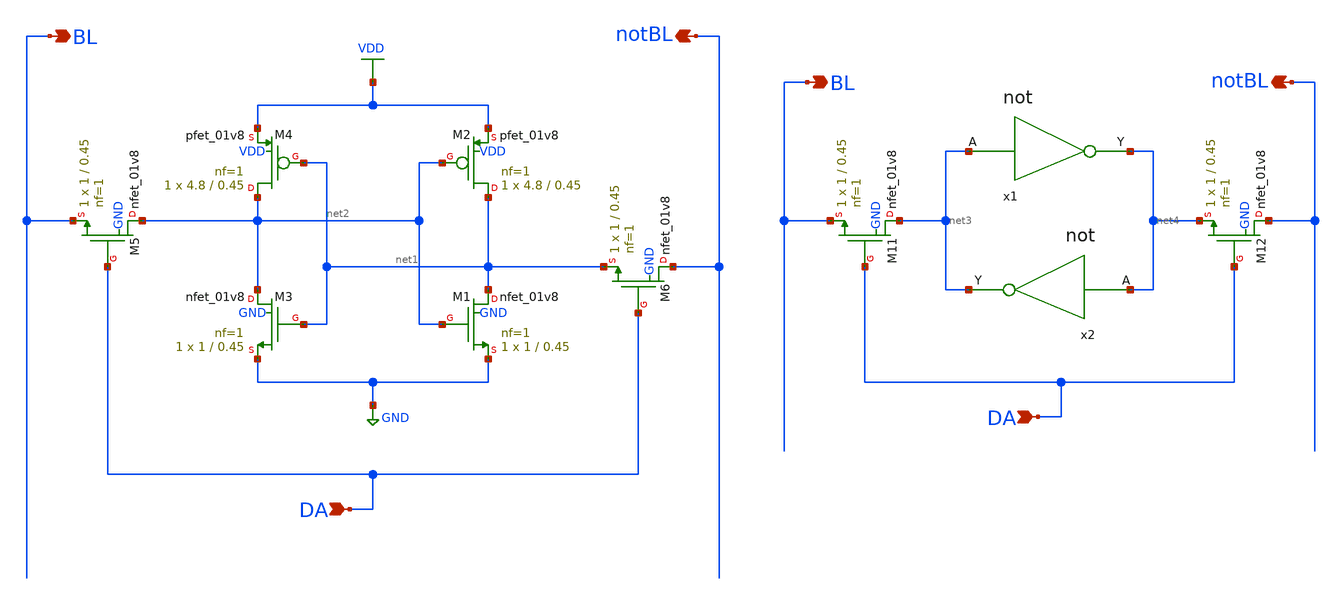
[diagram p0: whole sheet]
** sch_path: Circuiti/memories/s_RAM.sch
**.subckt s_RAM DA BL notBL DA BL notBL
*.ipin DA
*.opin BL
*.opin notBL
*.ipin DA
*.opin BL
*.opin notBL
XM1 net1 net2 GND GND sky130_fd_pr__nfet_01v8 L=0.45 W=1 nf=1 ad='int((nf+1)/2) * W/nf * 0.29' as='int((nf+2)/2) * W/nf * 0.29'
+ pd='2*int((nf+1)/2) * (W/nf + 0.29)' ps='2*int((nf+2)/2) * (W/nf + 0.29)' nrd='0.29 / W' nrs='0.29 / W'
+ sa=0 sb=0 sd=0 mult=1 m=1
XM2 net1 net2 VDD VDD sky130_fd_pr__pfet_01v8 L=0.45 W=4.8 nf=1 ad='int((nf+1)/2) * W/nf * 0.29' as='int((nf+2)/2) * W/nf * 0.29'
+ pd='2*int((nf+1)/2) * (W/nf + 0.29)' ps='2*int((nf+2)/2) * (W/nf + 0.29)' nrd='0.29 / W' nrs='0.29 / W'
+ sa=0 sb=0 sd=0 mult=1 m=1
XM3 net2 net1 GND GND sky130_fd_pr__nfet_01v8 L=0.45 W=1 nf=1 ad='int((nf+1)/2) * W/nf * 0.29' as='int((nf+2)/2) * W/nf * 0.29'
+ pd='2*int((nf+1)/2) * (W/nf + 0.29)' ps='2*int((nf+2)/2) * (W/nf + 0.29)' nrd='0.29 / W' nrs='0.29 / W'
+ sa=0 sb=0 sd=0 mult=1 m=1
XM4 net2 net1 VDD VDD sky130_fd_pr__pfet_01v8 L=0.45 W=4.8 nf=1 ad='int((nf+1)/2) * W/nf * 0.29' as='int((nf+2)/2) * W/nf * 0.29'
+ pd='2*int((nf+1)/2) * (W/nf + 0.29)' ps='2*int((nf+2)/2) * (W/nf + 0.29)' nrd='0.29 / W' nrs='0.29 / W'
+ sa=0 sb=0 sd=0 mult=1 m=1
XM5 net2 DA BL GND sky130_fd_pr__nfet_01v8 L=0.45 W=1 nf=1 ad='int((nf+1)/2) * W/nf * 0.29' as='int((nf+2)/2) * W/nf * 0.29'
+ pd='2*int((nf+1)/2) * (W/nf + 0.29)' ps='2*int((nf+2)/2) * (W/nf + 0.29)' nrd='0.29 / W' nrs='0.29 / W'
+ sa=0 sb=0 sd=0 mult=1 m=1
XM6 notBL DA net1 GND sky130_fd_pr__nfet_01v8 L=0.45 W=1 nf=1 ad='int((nf+1)/2) * W/nf * 0.29' as='int((nf+2)/2) * W/nf * 0.29'
+ pd='2*int((nf+1)/2) * (W/nf + 0.29)' ps='2*int((nf+2)/2) * (W/nf + 0.29)' nrd='0.29 / W' nrs='0.29 / W'
+ sa=0 sb=0 sd=0 mult=1 m=1
XM11 net3 DA BL GND sky130_fd_pr__nfet_01v8 L=0.45 W=1 nf=1 ad='int((nf+1)/2) * W/nf * 0.29' as='int((nf+2)/2) * W/nf * 0.29'
+ pd='2*int((nf+1)/2) * (W/nf + 0.29)' ps='2*int((nf+2)/2) * (W/nf + 0.29)' nrd='0.29 / W' nrs='0.29 / W'
+ sa=0 sb=0 sd=0 mult=1 m=1
XM12 notBL DA net4 GND sky130_fd_pr__nfet_01v8 L=0.45 W=1 nf=1 ad='int((nf+1)/2) * W/nf * 0.29' as='int((nf+2)/2) * W/nf * 0.29'
+ pd='2*int((nf+1)/2) * (W/nf + 0.29)' ps='2*int((nf+2)/2) * (W/nf + 0.29)' nrd='0.29 / W' nrs='0.29 / W'
+ sa=0 sb=0 sd=0 mult=1 m=1
x1 net3 net4 not
x2 net4 net3 not
**.ends

* expanding   symbol:  /home/matteo/Documenti/tesi/Circuiti/logic_gates_sch_sym/not.sym # of pins=2
** sym_path: Circuiti/logic_gates_sch_sym/not.sym
** sch_path: Circuiti/logic_gates_sch_sym/not.sch
.subckt not A Y
*.ipin A
*.opin Y
XM1 Y A GND GND sky130_fd_pr__nfet_01v8 L=0.45 W=1 nf=1 ad='int((nf+1)/2) * W/nf * 0.29' as='int((nf+2)/2) * W/nf * 0.29'
+ pd='2*int((nf+1)/2) * (W/nf + 0.29)' ps='2*int((nf+2)/2) * (W/nf + 0.29)' nrd='0.29 / W' nrs='0.29 / W'
+ sa=0 sb=0 sd=0 mult=1 m=1
XM2 Y A Vdd VDD sky130_fd_pr__pfet_01v8 L=0.45 W=4.8 nf=1 ad='int((nf+1)/2) * W/nf * 0.29' as='int((nf+2)/2) * W/nf * 0.29'
+ pd='2*int((nf+1)/2) * (W/nf + 0.29)' ps='2*int((nf+2)/2) * (W/nf + 0.29)' nrd='0.29 / W' nrs='0.29 / W'
+ sa=0 sb=0 sd=0 mult=1 m=1
.ends

.GLOBAL GND
.GLOBAL VDD
.GLOBAL Vdd
.end
